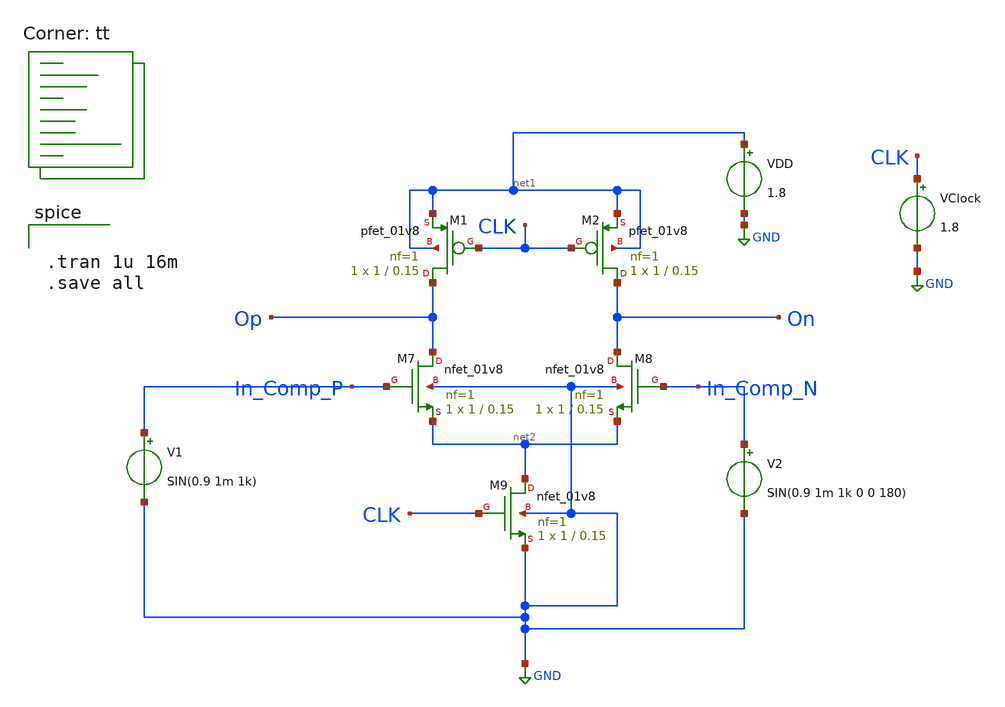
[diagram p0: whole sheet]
** sch_path: test_amp.sch
**.subckt test_amp
XM1 Op CLK net1 net1 sky130_fd_pr__pfet_01v8 L=0.15 W=1 nf=1 ad='int((nf+1)/2) * W/nf * 0.29' as='int((nf+2)/2) * W/nf * 0.29'
+ pd='2*int((nf+1)/2) * (W/nf + 0.29)' ps='2*int((nf+2)/2) * (W/nf + 0.29)' nrd='0.29 / W' nrs='0.29 / W'
+ sa=0 sb=0 sd=0 mult=1 m=1
XM2 On CLK net1 net1 sky130_fd_pr__pfet_01v8 L=0.15 W=1 nf=1 ad='int((nf+1)/2) * W/nf * 0.29' as='int((nf+2)/2) * W/nf * 0.29'
+ pd='2*int((nf+1)/2) * (W/nf + 0.29)' ps='2*int((nf+2)/2) * (W/nf + 0.29)' nrd='0.29 / W' nrs='0.29 / W'
+ sa=0 sb=0 sd=0 mult=1 m=1
XM7 Op In_Comp_P net2 GND sky130_fd_pr__nfet_01v8 L=0.15 W=1 nf=1 ad='int((nf+1)/2) * W/nf * 0.29' as='int((nf+2)/2) * W/nf * 0.29'
+ pd='2*int((nf+1)/2) * (W/nf + 0.29)' ps='2*int((nf+2)/2) * (W/nf + 0.29)' nrd='0.29 / W' nrs='0.29 / W'
+ sa=0 sb=0 sd=0 mult=1 m=1
XM8 On In_Comp_N net2 GND sky130_fd_pr__nfet_01v8 L=0.15 W=1 nf=1 ad='int((nf+1)/2) * W/nf * 0.29' as='int((nf+2)/2) * W/nf * 0.29'
+ pd='2*int((nf+1)/2) * (W/nf + 0.29)' ps='2*int((nf+2)/2) * (W/nf + 0.29)' nrd='0.29 / W' nrs='0.29 / W'
+ sa=0 sb=0 sd=0 mult=1 m=1
XM9 net2 CLK GND GND sky130_fd_pr__nfet_01v8 L=0.15 W=1 nf=1 ad='int((nf+1)/2) * W/nf * 0.29' as='int((nf+2)/2) * W/nf * 0.29'
+ pd='2*int((nf+1)/2) * (W/nf + 0.29)' ps='2*int((nf+2)/2) * (W/nf + 0.29)' nrd='0.29 / W' nrs='0.29 / W'
+ sa=0 sb=0 sd=0 mult=1 m=1
VClock CLK GND 1.8
VDD net1 GND 1.8
V1 In_Comp_P GND SIN(0.9 1m 1k)
V2 In_Comp_N GND SIN(0.9 1m 1k 0 0 180)
**** begin user architecture code
.lib $::SKYWATER_MODELS/sky130.lib.spice tt


.tran 1u 16m
.save all

**** end user architecture code
**.ends
.GLOBAL GND
.end
